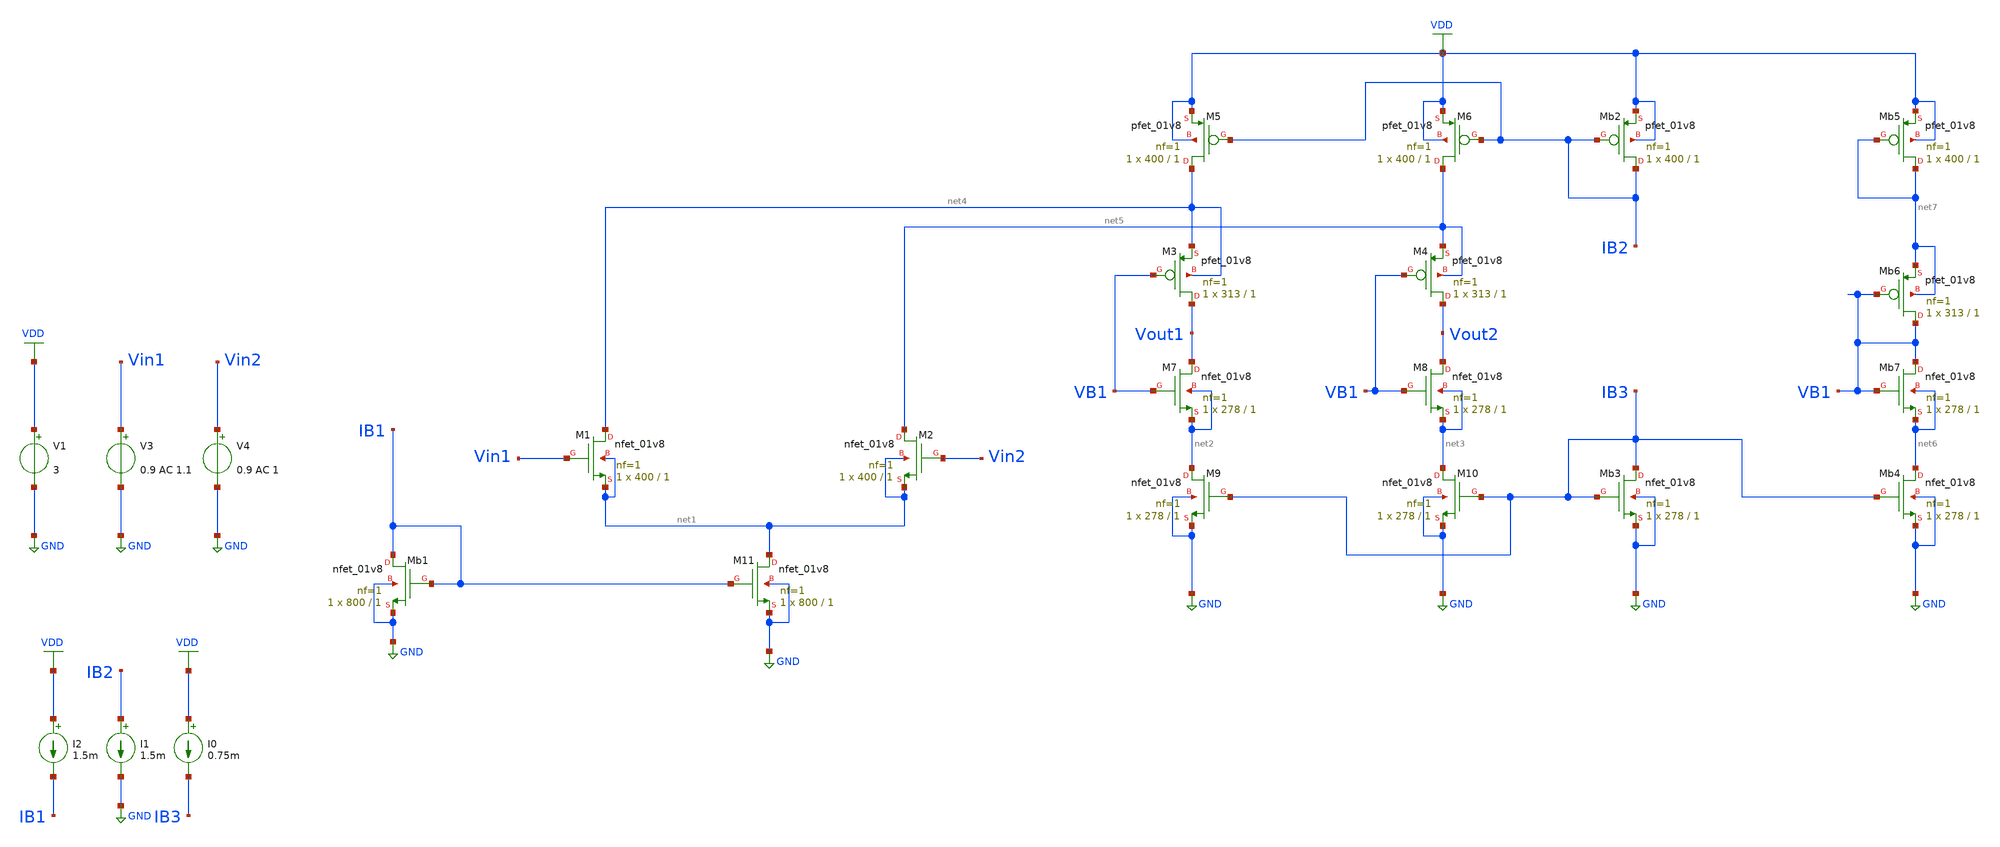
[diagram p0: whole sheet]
** sch_path: Circuits/Examples/Analog/Folded_Cascode/Folded_Cascode_v1.sch
**.subckt Folded_Cascode_v1
V1 VDD GND 3
XM11 net1 IB1 GND GND sky130_fd_pr__nfet_01v8 L=1 W=800 nf=1 ad='int((nf+1)/2) * W/nf * 0.29' as='int((nf+2)/2) * W/nf * 0.29'
+ pd='2*int((nf+1)/2) * (W/nf + 0.29)' ps='2*int((nf+2)/2) * (W/nf + 0.29)' nrd='0.29 / W' nrs='0.29 / W'
+ sa=0 sb=0 sd=0 mult=1 m=1
XM1 net4 Vin1 net1 net1 sky130_fd_pr__nfet_01v8 L=1 W=400 nf=1 ad='int((nf+1)/2) * W/nf * 0.29' as='int((nf+2)/2) * W/nf * 0.29'
+ pd='2*int((nf+1)/2) * (W/nf + 0.29)' ps='2*int((nf+2)/2) * (W/nf + 0.29)' nrd='0.29 / W' nrs='0.29 / W'
+ sa=0 sb=0 sd=0 mult=1 m=1
XM2 net5 Vin2 net1 net1 sky130_fd_pr__nfet_01v8 L=1 W=400 nf=1 ad='int((nf+1)/2) * W/nf * 0.29' as='int((nf+2)/2) * W/nf * 0.29'
+ pd='2*int((nf+1)/2) * (W/nf + 0.29)' ps='2*int((nf+2)/2) * (W/nf + 0.29)' nrd='0.29 / W' nrs='0.29 / W'
+ sa=0 sb=0 sd=0 mult=1 m=1
XM9 net2 IB3 GND GND sky130_fd_pr__nfet_01v8 L=1 W=278 nf=1 ad='int((nf+1)/2) * W/nf * 0.29' as='int((nf+2)/2) * W/nf * 0.29'
+ pd='2*int((nf+1)/2) * (W/nf + 0.29)' ps='2*int((nf+2)/2) * (W/nf + 0.29)' nrd='0.29 / W' nrs='0.29 / W'
+ sa=0 sb=0 sd=0 mult=1 m=1
XM10 net3 IB3 GND GND sky130_fd_pr__nfet_01v8 L=1 W=278 nf=1 ad='int((nf+1)/2) * W/nf * 0.29' as='int((nf+2)/2) * W/nf * 0.29'
+ pd='2*int((nf+1)/2) * (W/nf + 0.29)' ps='2*int((nf+2)/2) * (W/nf + 0.29)' nrd='0.29 / W' nrs='0.29 / W'
+ sa=0 sb=0 sd=0 mult=1 m=1
XM7 Vout1 VB1 net2 net2 sky130_fd_pr__nfet_01v8 L=1 W=278 nf=1 ad='int((nf+1)/2) * W/nf * 0.29' as='int((nf+2)/2) * W/nf * 0.29'
+ pd='2*int((nf+1)/2) * (W/nf + 0.29)' ps='2*int((nf+2)/2) * (W/nf + 0.29)' nrd='0.29 / W' nrs='0.29 / W'
+ sa=0 sb=0 sd=0 mult=1 m=1
XM8 Vout2 VB1 net3 net3 sky130_fd_pr__nfet_01v8 L=1 W=278 nf=1 ad='int((nf+1)/2) * W/nf * 0.29' as='int((nf+2)/2) * W/nf * 0.29'
+ pd='2*int((nf+1)/2) * (W/nf + 0.29)' ps='2*int((nf+2)/2) * (W/nf + 0.29)' nrd='0.29 / W' nrs='0.29 / W'
+ sa=0 sb=0 sd=0 mult=1 m=1
XM3 Vout1 VB1 net4 net4 sky130_fd_pr__pfet_01v8 L=1 W=313 nf=1 ad='int((nf+1)/2) * W/nf * 0.29' as='int((nf+2)/2) * W/nf * 0.29'
+ pd='2*int((nf+1)/2) * (W/nf + 0.29)' ps='2*int((nf+2)/2) * (W/nf + 0.29)' nrd='0.29 / W' nrs='0.29 / W'
+ sa=0 sb=0 sd=0 mult=1 m=1
XM4 Vout2 VB1 net5 net5 sky130_fd_pr__pfet_01v8 L=1 W=313 nf=1 ad='int((nf+1)/2) * W/nf * 0.29' as='int((nf+2)/2) * W/nf * 0.29'
+ pd='2*int((nf+1)/2) * (W/nf + 0.29)' ps='2*int((nf+2)/2) * (W/nf + 0.29)' nrd='0.29 / W' nrs='0.29 / W'
+ sa=0 sb=0 sd=0 mult=1 m=1
XM5 net4 IB2 VDD VDD sky130_fd_pr__pfet_01v8 L=1 W=400 nf=1 ad='int((nf+1)/2) * W/nf * 0.29' as='int((nf+2)/2) * W/nf * 0.29'
+ pd='2*int((nf+1)/2) * (W/nf + 0.29)' ps='2*int((nf+2)/2) * (W/nf + 0.29)' nrd='0.29 / W' nrs='0.29 / W'
+ sa=0 sb=0 sd=0 mult=1 m=1
XM6 net5 IB2 VDD VDD sky130_fd_pr__pfet_01v8 L=1 W=400 nf=1 ad='int((nf+1)/2) * W/nf * 0.29' as='int((nf+2)/2) * W/nf * 0.29'
+ pd='2*int((nf+1)/2) * (W/nf + 0.29)' ps='2*int((nf+2)/2) * (W/nf + 0.29)' nrd='0.29 / W' nrs='0.29 / W'
+ sa=0 sb=0 sd=0 mult=1 m=1
XMb2 IB2 IB2 VDD VDD sky130_fd_pr__pfet_01v8 L=1 W=400 nf=1 ad='int((nf+1)/2) * W/nf * 0.29' as='int((nf+2)/2) * W/nf * 0.29'
+ pd='2*int((nf+1)/2) * (W/nf + 0.29)' ps='2*int((nf+2)/2) * (W/nf + 0.29)' nrd='0.29 / W' nrs='0.29 / W'
+ sa=0 sb=0 sd=0 mult=1 m=1
XMb3 IB3 IB3 GND GND sky130_fd_pr__nfet_01v8 L=1 W=278 nf=1 ad='int((nf+1)/2) * W/nf * 0.29' as='int((nf+2)/2) * W/nf * 0.29'
+ pd='2*int((nf+1)/2) * (W/nf + 0.29)' ps='2*int((nf+2)/2) * (W/nf + 0.29)' nrd='0.29 / W' nrs='0.29 / W'
+ sa=0 sb=0 sd=0 mult=1 m=1
XMb1 IB1 IB1 GND GND sky130_fd_pr__nfet_01v8 L=1 W=800 nf=1 ad='int((nf+1)/2) * W/nf * 0.29' as='int((nf+2)/2) * W/nf * 0.29'
+ pd='2*int((nf+1)/2) * (W/nf + 0.29)' ps='2*int((nf+2)/2) * (W/nf + 0.29)' nrd='0.29 / W' nrs='0.29 / W'
+ sa=0 sb=0 sd=0 mult=1 m=1
I0 VDD IB3 0.75m
I1 IB2 GND 1.5m
I2 VDD IB1 1.5m
V3 Vin1 GND 0.9 AC 1.1
V4 Vin2 GND 0.9 AC 1
XMb4 net6 IB3 GND GND sky130_fd_pr__nfet_01v8 L=1 W=278 nf=1 ad='int((nf+1)/2) * W/nf * 0.29' as='int((nf+2)/2) * W/nf * 0.29'
+ pd='2*int((nf+1)/2) * (W/nf + 0.29)' ps='2*int((nf+2)/2) * (W/nf + 0.29)' nrd='0.29 / W' nrs='0.29 / W'
+ sa=0 sb=0 sd=0 mult=1 m=1
XMb7 VB1 VB1 net6 net6 sky130_fd_pr__nfet_01v8 L=1 W=278 nf=1 ad='int((nf+1)/2) * W/nf * 0.29' as='int((nf+2)/2) * W/nf * 0.29'
+ pd='2*int((nf+1)/2) * (W/nf + 0.29)' ps='2*int((nf+2)/2) * (W/nf + 0.29)' nrd='0.29 / W' nrs='0.29 / W'
+ sa=0 sb=0 sd=0 mult=1 m=1
XMb6 VB1 VB1 net7 net7 sky130_fd_pr__pfet_01v8 L=1 W=313 nf=1 ad='int((nf+1)/2) * W/nf * 0.29' as='int((nf+2)/2) * W/nf * 0.29'
+ pd='2*int((nf+1)/2) * (W/nf + 0.29)' ps='2*int((nf+2)/2) * (W/nf + 0.29)' nrd='0.29 / W' nrs='0.29 / W'
+ sa=0 sb=0 sd=0 mult=1 m=1
XMb5 net7 net7 VDD VDD sky130_fd_pr__pfet_01v8 L=1 W=400 nf=1 ad='int((nf+1)/2) * W/nf * 0.29' as='int((nf+2)/2) * W/nf * 0.29'
+ pd='2*int((nf+1)/2) * (W/nf + 0.29)' ps='2*int((nf+2)/2) * (W/nf + 0.29)' nrd='0.29 / W' nrs='0.29 / W'
+ sa=0 sb=0 sd=0 mult=1 m=1
**** begin user architecture code
 ** manual skywater pdks install (with patches applied)
* .lib $::SKYWATER_MODELS/models/sky130.lib.spice tt

** opencircuitdesign pdks install
.lib $::SKYWATER_MODELS/sky130.lib.spice tt

.param mc_mm_switch=0
.param mc_pr_switch=0


.ac dec 20 1 1e16
.control
run
plot db(Vout2-Vout1)
.endc
.save all

**** end user architecture code
**.ends
.GLOBAL GND
.GLOBAL VDD
.end
